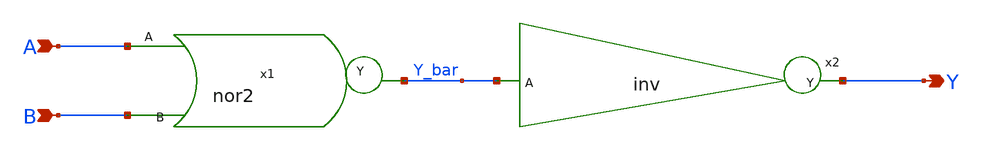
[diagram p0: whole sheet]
** sch_path: eng331lab_final/eng331lab_xschem/or2.sch
**.subckt or2 A B Y
*.ipin A
*.ipin B
*.opin Y
x1 A B Y_bar nor2
x2 Y Y_bar inv
**.ends

* expanding   symbol:  eng331_debug/eng331lab_xschem/nor2.sym # of pins=3
** sym_path: eng331lab_final/eng331lab_xschem/nor2.sym
** sch_path: eng331lab_final/eng331lab_xschem/nor2.sch
.subckt nor2 A B Y
*.ipin A
*.ipin B
*.opin Y
XM1 net1 A VDD VDD sky130_fd_pr__pfet_01v8 L=0.15 W=1.6 nf=1 ad='int((1 + 1)/2) * 1.6 / 1 * 0.29' as='int((1 + 2)/2) * 1.6 / 1 * 0.29'
+ pd='2*int((1 + 1)/2) * (1.6 / 1 + 0.29)' ps='2*int((1 + 2)/2) * (1.6 / 1 + 0.29)' nrd='0.29 / 1.6 ' nrs='0.29 / 1.6 '
+ sa=0 sb=0 sd=0 mult=1 m=1
XM2 Y B net1 VDD sky130_fd_pr__pfet_01v8 L=0.15 W=1.6 nf=1 ad='int((1 + 1)/2) * 1.6 / 1 * 0.29' as='int((1 + 2)/2) * 1.6 / 1 * 0.29'
+ pd='2*int((1 + 1)/2) * (1.6 / 1 + 0.29)' ps='2*int((1 + 2)/2) * (1.6 / 1 + 0.29)' nrd='0.29 / 1.6 ' nrs='0.29 / 1.6 '
+ sa=0 sb=0 sd=0 mult=1 m=1
XM3 Y A GND GND sky130_fd_pr__nfet_01v8 L=0.15 W=0.5 nf=1 ad='int((1 + 1)/2) * 0.5 / 1 * 0.29' as='int((1 + 2)/2) * 0.5 / 1 * 0.29'
+ pd='2*int((1 + 1)/2) * (0.5 / 1 + 0.29)' ps='2*int((1 + 2)/2) * (0.5 / 1 + 0.29)' nrd='0.29 / 0.5 ' nrs='0.29 / 0.5 '
+ sa=0 sb=0 sd=0 mult=1 m=1
XM4 Y B GND GND sky130_fd_pr__nfet_01v8 L=0.15 W=0.5 nf=1 ad='int((1 + 1)/2) * 0.5 / 1 * 0.29' as='int((1 + 2)/2) * 0.5 / 1 * 0.29'
+ pd='2*int((1 + 1)/2) * (0.5 / 1 + 0.29)' ps='2*int((1 + 2)/2) * (0.5 / 1 + 0.29)' nrd='0.29 / 0.5 ' nrs='0.29 / 0.5 '
+ sa=0 sb=0 sd=0 mult=1 m=1
.ends


* expanding   symbol:  eng331_debug/eng331lab_xschem/inv.sym # of pins=2
** sym_path: eng331lab_final/eng331lab_xschem/inv.sym
** sch_path: eng331lab_final/eng331lab_xschem/inv.sch
.subckt inv Y A
*.ipin A
*.opin Y
XM1 Y A VDD VDD sky130_fd_pr__pfet_01v8 L=0.15 W=0.8 nf=1 ad='int((1 + 1)/2) * 0.8 / 1 * 0.29' as='int((1 + 2)/2) * 0.8 / 1 * 0.29'
+ pd='2*int((1 + 1)/2) * (0.8 / 1 + 0.29)' ps='2*int((1 + 2)/2) * (0.8 / 1 + 0.29)' nrd='0.29 / 0.8 ' nrs='0.29 / 0.8 '
+ sa=0 sb=0 sd=0 mult=1 m=1
XM2 Y A GND GND sky130_fd_pr__nfet_01v8 L=0.15 W=0.5 nf=1 ad='int((1 + 1)/2) * 0.5 / 1 * 0.29' as='int((1 + 2)/2) * 0.5 / 1 * 0.29'
+ pd='2*int((1 + 1)/2) * (0.5 / 1 + 0.29)' ps='2*int((1 + 2)/2) * (0.5 / 1 + 0.29)' nrd='0.29 / 0.5 ' nrs='0.29 / 0.5 '
+ sa=0 sb=0 sd=0 mult=1 m=1
.ends

.GLOBAL VDD
.GLOBAL GND
.end
